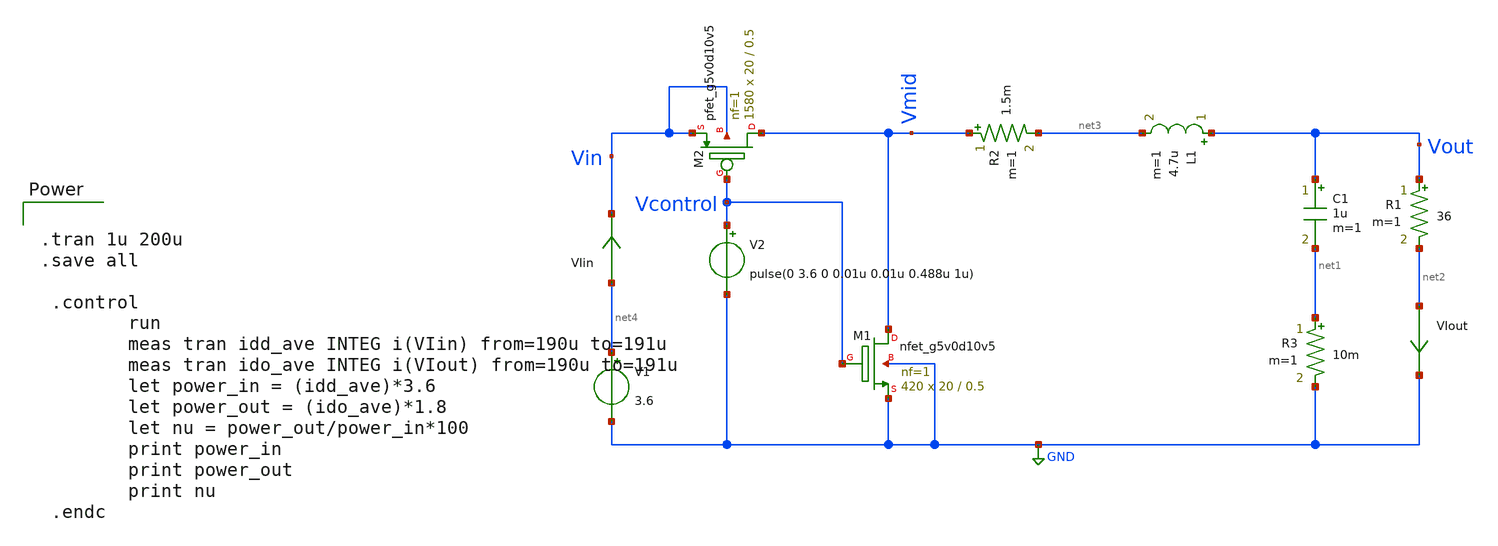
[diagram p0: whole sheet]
** sch_path: Abishek_Sam_group/Buck_converter.sch
**.subckt Buck_converter
XM1 Vmid Vcontrol GND GND sky130_fd_pr__nfet_g5v0d10v5 L=0.5 W=20 nf=1 ad='int((nf+1)/2) * W/nf * 0.29'
+ as='int((nf+2)/2) * W/nf * 0.29' pd='2*int((nf+1)/2) * (W/nf + 0.29)' ps='2*int((nf+2)/2) * (W/nf + 0.29)'
+ nrd='0.29 / W' nrs='0.29 / W' sa=0 sb=0 sd=0 mult=420 m=420
XM2 Vmid Vcontrol Vin Vin sky130_fd_pr__pfet_g5v0d10v5 L=0.5 W=20 nf=1 ad='int((nf+1)/2) * W/nf * 0.29'
+ as='int((nf+2)/2) * W/nf * 0.29' pd='2*int((nf+1)/2) * (W/nf + 0.29)' ps='2*int((nf+2)/2) * (W/nf + 0.29)'
+ nrd='0.29 / W' nrs='0.29 / W' sa=0 sb=0 sd=0 mult=1580 m=1580
C1 Vout net1 1u m=1
L1 Vout net3 4.7u m=1
R1 Vout net2 36 m=1
V1 net4 GND 3.6
R2 Vmid net3 1.5m m=1
R3 net1 GND 10m m=1
V2 Vcontrol GND pulse(0 3.6 0 0.01u 0.01u 0.488u 1u)
VIout net2 GND 0
.save i(viout)
VIin net4 Vin 0
.save i(viin)
**** begin user architecture code

.lib $::SKYWATER_MODELS/sky130.lib.spice tt

**** end user architecture code
**.ends
.GLOBAL GND
**** begin user architecture code


.tran 1u 200u
.save all

 .control
        run
        meas tran idd_ave INTEG i(VIin) from=190u to=191u
        meas tran ido_ave INTEG i(VIout) from=190u to=191u
        let power_in = (idd_ave)*3.6
        let power_out = (ido_ave)*1.8
        let nu = power_out/power_in*100
        print power_in
        print power_out
        print nu
 .endc


**** end user architecture code
.end
